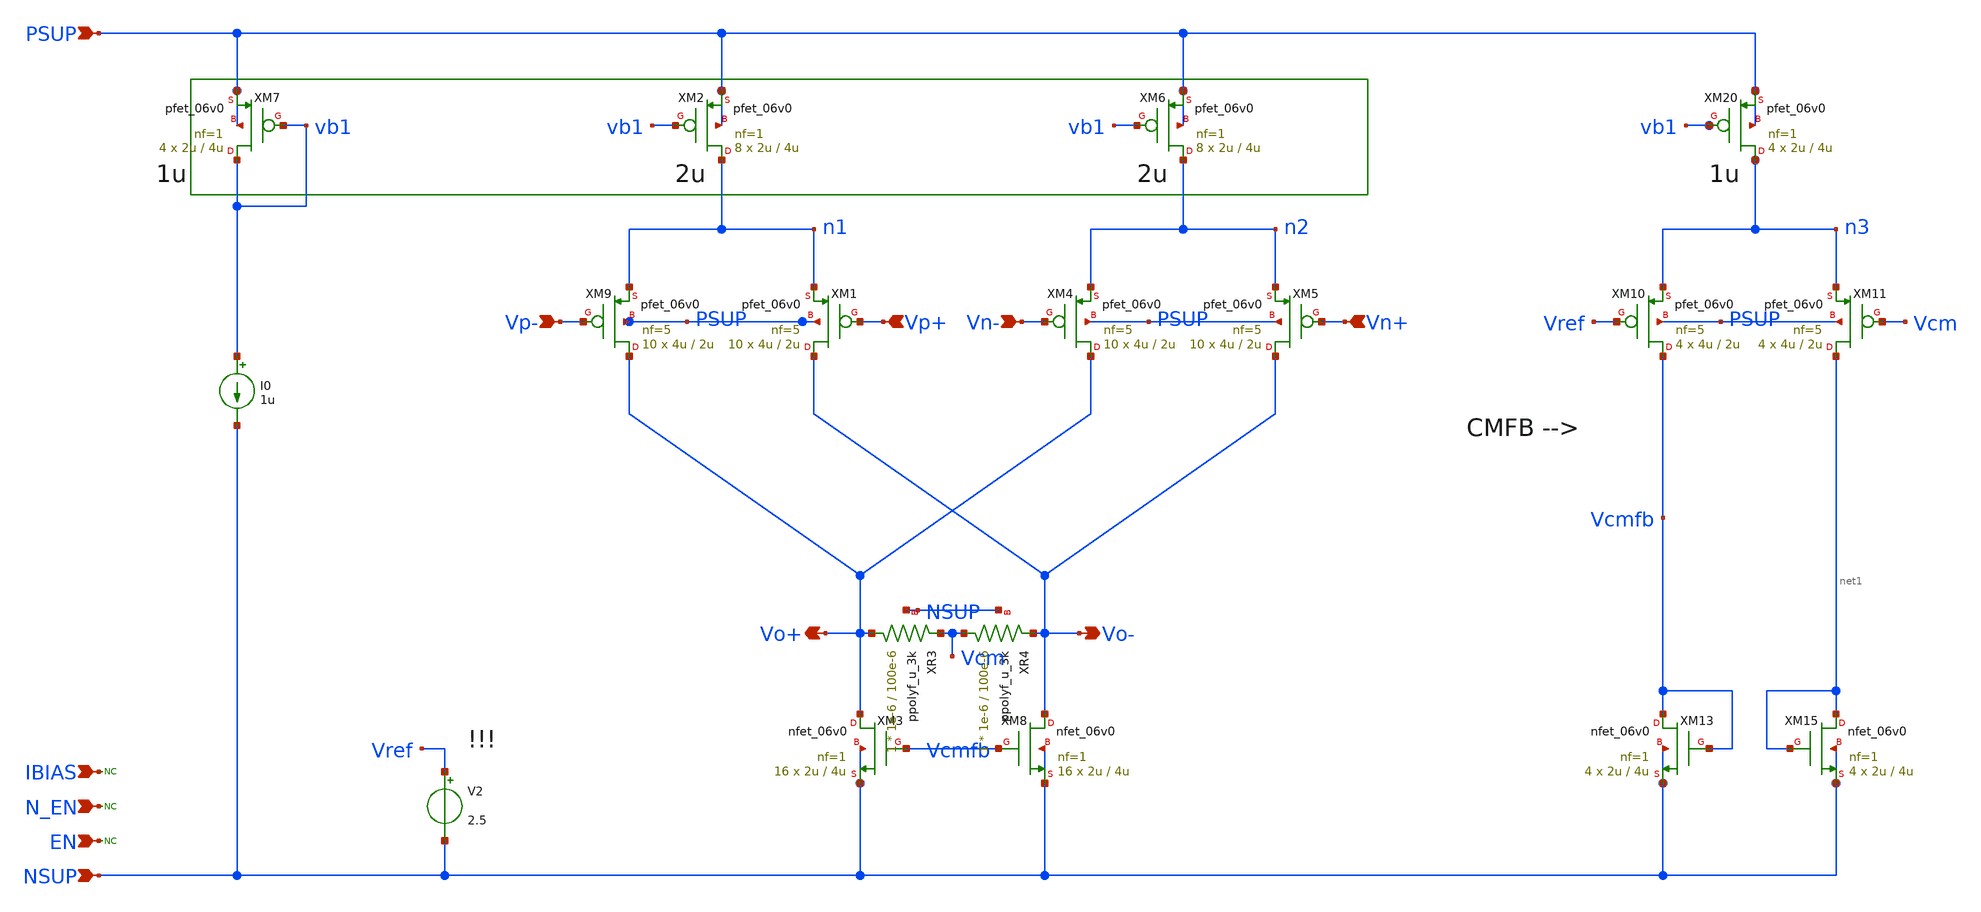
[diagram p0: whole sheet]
** sch_path: xschem/blocks/fdda/fdda_lo_z.sch
**.subckt fdda_lo_z PSUP NSUP N_EN EN IBIAS Vp+ Vp- Vn+ Vn- Vo- Vo+
*.ipin PSUP
*.ipin NSUP
*.ipin N_EN
*.ipin EN
*.ipin IBIAS
*.ipin Vp+
*.ipin Vp-
*.ipin Vn+
*.ipin Vn-
*.opin Vo-
*.opin Vo+
* noconn N_EN
* noconn EN
I0 vb1 NSUP 1u
XM9 Vo+ Vp- n1 PSUP pfet_06v0 L=2u W=4u nf=5 ad='int((nf+1)/2) * W/nf * 0.18u' as='int((nf+2)/2) * W/nf * 0.18u'
+ pd='2*int((nf+1)/2) * (W/nf + 0.18u)' ps='2*int((nf+2)/2) * (W/nf + 0.18u)' nrd='0.18u / W' nrs='0.18u / W'
+ sa=0 sb=0 sd=0 m=10
XM1 Vo- Vp+ n1 PSUP pfet_06v0 L=2u W=4u nf=5 ad='int((nf+1)/2) * W/nf * 0.18u' as='int((nf+2)/2) * W/nf * 0.18u'
+ pd='2*int((nf+1)/2) * (W/nf + 0.18u)' ps='2*int((nf+2)/2) * (W/nf + 0.18u)' nrd='0.18u / W' nrs='0.18u / W'
+ sa=0 sb=0 sd=0 m=10
XM2 n1 vb1 PSUP PSUP pfet_06v0 L=4u W=2u nf=1 ad='int((nf+1)/2) * W/nf * 0.18u' as='int((nf+2)/2) * W/nf * 0.18u'
+ pd='2*int((nf+1)/2) * (W/nf + 0.18u)' ps='2*int((nf+2)/2) * (W/nf + 0.18u)' nrd='0.18u / W' nrs='0.18u / W'
+ sa=0 sb=0 sd=0 m=8
XM3 Vo+ Vcmfb NSUP NSUP nfet_06v0 L=4u W=2u nf=1 ad='int((nf+1)/2) * W/nf * 0.18u' as='int((nf+2)/2) * W/nf * 0.18u'
+ pd='2*int((nf+1)/2) * (W/nf + 0.18u)' ps='2*int((nf+2)/2) * (W/nf + 0.18u)' nrd='0.18u / W' nrs='0.18u / W'
+ sa=0 sb=0 sd=0 m=16
XM6 n2 vb1 PSUP PSUP pfet_06v0 L=4u W=2u nf=1 ad='int((nf+1)/2) * W/nf * 0.18u' as='int((nf+2)/2) * W/nf * 0.18u'
+ pd='2*int((nf+1)/2) * (W/nf + 0.18u)' ps='2*int((nf+2)/2) * (W/nf + 0.18u)' nrd='0.18u / W' nrs='0.18u / W'
+ sa=0 sb=0 sd=0 m=8
XM8 Vo- Vcmfb NSUP NSUP nfet_06v0 L=4u W=2u nf=1 ad='int((nf+1)/2) * W/nf * 0.18u' as='int((nf+2)/2) * W/nf * 0.18u'
+ pd='2*int((nf+1)/2) * (W/nf + 0.18u)' ps='2*int((nf+2)/2) * (W/nf + 0.18u)' nrd='0.18u / W' nrs='0.18u / W'
+ sa=0 sb=0 sd=0 m=16
XM7 vb1 vb1 PSUP PSUP pfet_06v0 L=4u W=2u nf=1 ad='int((nf+1)/2) * W/nf * 0.18u' as='int((nf+2)/2) * W/nf * 0.18u'
+ pd='2*int((nf+1)/2) * (W/nf + 0.18u)' ps='2*int((nf+2)/2) * (W/nf + 0.18u)' nrd='0.18u / W' nrs='0.18u / W'
+ sa=0 sb=0 sd=0 m=4
* noconn IBIAS
XM13 Vcmfb Vcmfb NSUP NSUP nfet_06v0 L=4u W=2u nf=1 ad='int((nf+1)/2) * W/nf * 0.18u' as='int((nf+2)/2) * W/nf * 0.18u'
+ pd='2*int((nf+1)/2) * (W/nf + 0.18u)' ps='2*int((nf+2)/2) * (W/nf + 0.18u)' nrd='0.18u / W' nrs='0.18u / W'
+ sa=0 sb=0 sd=0 m=4
XM15 net1 net1 NSUP NSUP nfet_06v0 L=4u W=2u nf=1 ad='int((nf+1)/2) * W/nf * 0.18u' as='int((nf+2)/2) * W/nf * 0.18u'
+ pd='2*int((nf+1)/2) * (W/nf + 0.18u)' ps='2*int((nf+2)/2) * (W/nf + 0.18u)' nrd='0.18u / W' nrs='0.18u / W'
+ sa=0 sb=0 sd=0 m=4
V2 Vref NSUP 2.5
XM20 n3 vb1 PSUP PSUP pfet_06v0 L=4u W=2u nf=1 ad='int((nf+1)/2) * W/nf * 0.18u' as='int((nf+2)/2) * W/nf * 0.18u'
+ pd='2*int((nf+1)/2) * (W/nf + 0.18u)' ps='2*int((nf+2)/2) * (W/nf + 0.18u)' nrd='0.18u / W' nrs='0.18u / W'
+ sa=0 sb=0 sd=0 m=4
XM10 Vcmfb Vref n3 PSUP pfet_06v0 L=2u W=4u nf=5 ad='int((nf+1)/2) * W/nf * 0.18u' as='int((nf+2)/2) * W/nf * 0.18u'
+ pd='2*int((nf+1)/2) * (W/nf + 0.18u)' ps='2*int((nf+2)/2) * (W/nf + 0.18u)' nrd='0.18u / W' nrs='0.18u / W'
+ sa=0 sb=0 sd=0 m=4
XM11 net1 Vcm n3 PSUP pfet_06v0 L=2u W=4u nf=5 ad='int((nf+1)/2) * W/nf * 0.18u' as='int((nf+2)/2) * W/nf * 0.18u'
+ pd='2*int((nf+1)/2) * (W/nf + 0.18u)' ps='2*int((nf+2)/2) * (W/nf + 0.18u)' nrd='0.18u / W' nrs='0.18u / W'
+ sa=0 sb=0 sd=0 m=4
XM4 Vo+ Vn- n2 PSUP pfet_06v0 L=2u W=4u nf=5 ad='int((nf+1)/2) * W/nf * 0.18u' as='int((nf+2)/2) * W/nf * 0.18u'
+ pd='2*int((nf+1)/2) * (W/nf + 0.18u)' ps='2*int((nf+2)/2) * (W/nf + 0.18u)' nrd='0.18u / W' nrs='0.18u / W'
+ sa=0 sb=0 sd=0 m=10
XM5 Vo- Vn+ n2 PSUP pfet_06v0 L=2u W=4u nf=5 ad='int((nf+1)/2) * W/nf * 0.18u' as='int((nf+2)/2) * W/nf * 0.18u'
+ pd='2*int((nf+1)/2) * (W/nf + 0.18u)' ps='2*int((nf+2)/2) * (W/nf + 0.18u)' nrd='0.18u / W' nrs='0.18u / W'
+ sa=0 sb=0 sd=0 m=10
XR3 Vo+ Vcm NSUP ppolyf_u_3k r_width=1e-6 r_length=100e-6 m=1
XR4 Vcm Vo- NSUP ppolyf_u_3k r_width=1e-6 r_length=100e-6 m=1
**.ends
.end
